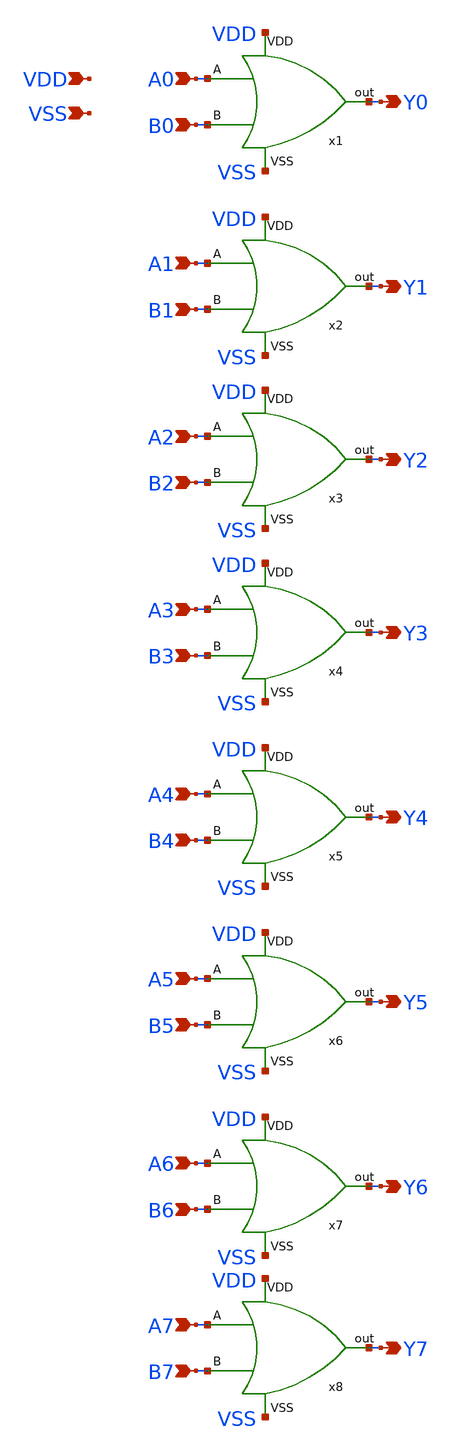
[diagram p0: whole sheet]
** sch_path: or/or2_8bit.sch
**.subckt or2_8bit A0 Y0 B0 VDD VSS A1 B1 Y1 A2 B2 Y2 A3 B3 Y3 A4 B4 Y4 A5 B5 Y5 Y6 A6 B6 B7 A7 Y7
*.ipin A0
*.opin Y0
*.ipin B0
*.ipin VDD
*.ipin VSS
*.ipin A1
*.ipin B1
*.opin Y1
*.ipin A2
*.ipin B2
*.opin Y2
*.ipin A3
*.ipin B3
*.opin Y3
*.ipin A4
*.ipin B4
*.opin Y4
*.ipin A5
*.ipin B5
*.opin Y5
*.opin Y6
*.ipin A6
*.ipin B6
*.ipin B7
*.ipin A7
*.opin Y7
x1 VSS VDD A0 B0 Y0 or2
x2 VSS VDD A1 B1 Y1 or2
x3 VSS VDD A2 B2 Y2 or2
x4 VSS VDD A3 B3 Y3 or2
x5 VSS VDD A4 B4 Y4 or2
x6 VSS VDD A5 B5 Y5 or2
x7 VSS VDD A6 B6 Y6 or2
x8 VSS VDD A7 B7 Y7 or2
**.ends
.end
